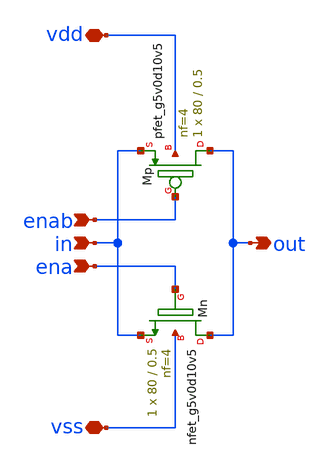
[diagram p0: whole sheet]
** sch_path: xschem/tgate.sch
**.subckt tgate enab ena in out vdd vss
*.ipin enab
*.ipin ena
*.ipin in
*.opin out
*.iopin vdd
*.iopin vss
XMn out ena in vss sky130_fd_pr__nfet_g5v0d10v5 L=0.5 W=80 nf=4 ad='int((nf+1)/2) * W/nf * 0.29' as='int((nf+2)/2) * W/nf * 0.29'
+ pd='2*int((nf+1)/2) * (W/nf + 0.29)' ps='2*int((nf+2)/2) * (W/nf + 0.29)' nrd='0.29 / W' nrs='0.29 / W'
+ sa=0 sb=0 sd=0 mult=1 m=1
XMp out enab in vdd sky130_fd_pr__pfet_g5v0d10v5 L=0.5 W=80 nf=4 ad='int((nf+1)/2) * W/nf * 0.29' as='int((nf+2)/2) * W/nf * 0.29'
+ pd='2*int((nf+1)/2) * (W/nf + 0.29)' ps='2*int((nf+2)/2) * (W/nf + 0.29)' nrd='0.29 / W' nrs='0.29 / W'
+ sa=0 sb=0 sd=0 mult=1 m=1
**.ends
.end
